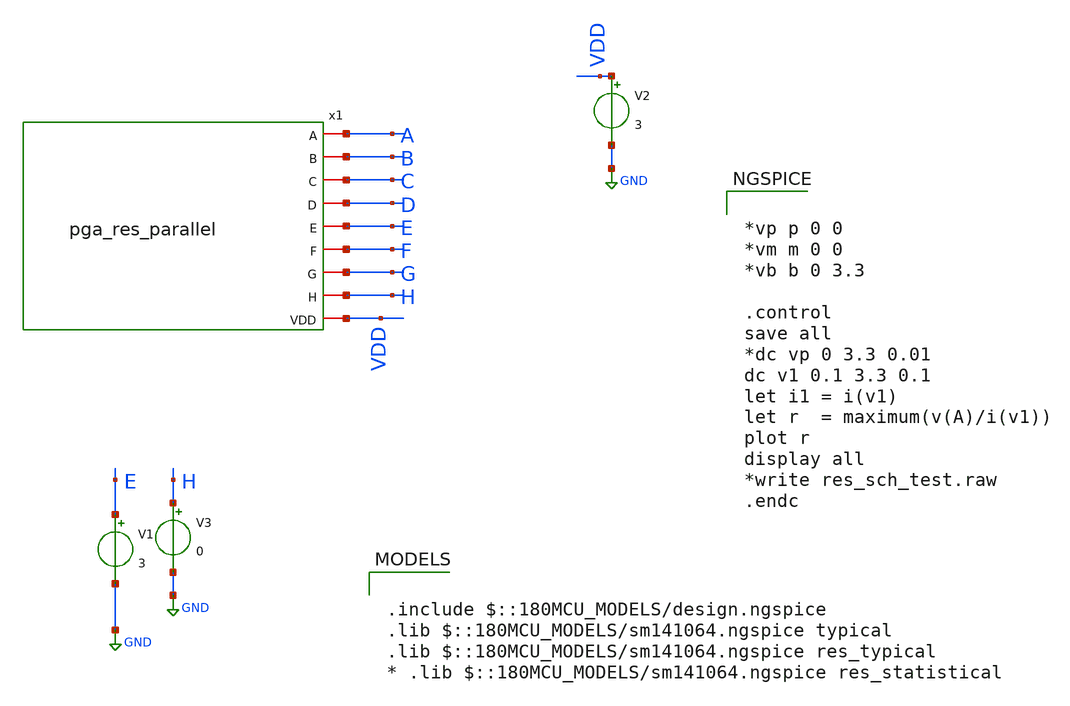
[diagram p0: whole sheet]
** sch_path: AWG_OUTPUT_AND_MUX_PAKISTAN_05/xschem/pga_parallel_tb.sch
**.subckt pga_parallel_tb
V1 E GND 3
V2 VDD GND 3
x1 A B C D E F G H VDD pga_res_parallel
V3 H GND 0
**** begin user architecture code

.include $::180MCU_MODELS/design.ngspice
.lib $::180MCU_MODELS/sm141064.ngspice typical
.lib $::180MCU_MODELS/sm141064.ngspice res_typical
* .lib $::180MCU_MODELS/sm141064.ngspice res_statistical



*vp p 0 0
*vm m 0 0
*vb b 0 3.3

.control
save all
*dc vp 0 3.3 0.01
dc v1 0.1 3.3 0.1
let i1 = i(v1)
let r  = maximum(v(A)/i(v1))
plot r
display all
*write res_sch_test.raw
.endc


**** end user architecture code
**.ends

* expanding   symbol:  pga_res_parallel.sym # of pins=9
** sym_path: AWG_OUTPUT_AND_MUX_PAKISTAN_05/xschem/pga_res_parallel.sym
** sch_path: AWG_OUTPUT_AND_MUX_PAKISTAN_05/xschem/pga_res_parallel.sch
.subckt pga_res_parallel A B C D E F G H VDD
*.iopin VDD
*.iopin A
*.iopin B
*.iopin C
*.iopin D
*.iopin E
*.iopin F
*.iopin G
*.iopin H
XR1 net1 A VDD ppolyf_u r_width=1e-6 r_length=1e-6 m=1
XR2 net2 net1 VDD ppolyf_u r_width=1e-6 r_length=1e-6 m=1
XR3 net2 net2 VDD ppolyf_u r_width=1e-6 r_length=1e-6 m=1
XR4 net2 net2 VDD ppolyf_u r_width=1e-6 r_length=1e-6 m=1
XR5 net6 net2 VDD ppolyf_u r_width=1e-6 r_length=1e-6 m=1
XR6 net3 net6 VDD ppolyf_u r_width=1e-6 r_length=1e-6 m=1
XR7 net4 net3 VDD ppolyf_u r_width=1e-6 r_length=1e-6 m=1
XR8 net7 net4 VDD ppolyf_u r_width=1e-6 r_length=1e-6 m=1
XR9 net5 net7 VDD ppolyf_u r_width=1e-6 r_length=1e-6 m=1
XR10 net78 net5 VDD ppolyf_u r_width=1e-6 r_length=1e-6 m=1
XR11 net8 net78 VDD ppolyf_u r_width=1e-6 r_length=1e-6 m=1
XR12 B net8 VDD ppolyf_u r_width=1e-6 r_length=1e-6 m=1
XR13 net9 B VDD ppolyf_u r_width=1e-6 r_length=1e-6 m=1
XR14 net14 net9 VDD ppolyf_u r_width=1e-6 r_length=1e-6 m=1
XR15 net10 net14 VDD ppolyf_u r_width=1e-6 r_length=1e-6 m=1
XR16 net11 net10 VDD ppolyf_u r_width=1e-6 r_length=1e-6 m=1
XR17 net15 net11 VDD ppolyf_u r_width=1e-6 r_length=1e-6 m=1
XR18 net12 net15 VDD ppolyf_u r_width=1e-6 r_length=1e-6 m=1
XR19 net13 net12 VDD ppolyf_u r_width=1e-6 r_length=1e-6 m=1
XR20 C net13 VDD ppolyf_u r_width=1e-6 r_length=1e-6 m=1
XR25 net16 C VDD ppolyf_u r_width=1e-6 r_length=1e-6 m=1
XR26 net22 net16 VDD ppolyf_u r_width=1e-6 r_length=1e-6 m=1
XR27 net17 net22 VDD ppolyf_u r_width=1e-6 r_length=1e-6 m=1
XR28 net18 net17 VDD ppolyf_u r_width=1e-6 r_length=1e-6 m=1
XR29 net23 net18 VDD ppolyf_u r_width=1e-6 r_length=1e-6 m=1
XR30 net19 net23 VDD ppolyf_u r_width=1e-6 r_length=1e-6 m=1
XR31 net20 net19 VDD ppolyf_u r_width=1e-6 r_length=1e-6 m=1
XR32 net24 net20 VDD ppolyf_u r_width=1e-6 r_length=1e-6 m=1
XR33 net21 net24 VDD ppolyf_u r_width=1e-6 r_length=1e-6 m=1
XR34 net79 net21 VDD ppolyf_u r_width=1e-6 r_length=1e-6 m=1
XR35 net25 net79 VDD ppolyf_u r_width=1e-6 r_length=1e-6 m=1
XR36 D net25 VDD ppolyf_u r_width=1e-6 r_length=1e-6 m=1
XR37 net26 D VDD ppolyf_u r_width=1e-6 r_length=1e-6 m=1
XR38 net32 net26 VDD ppolyf_u r_width=1e-6 r_length=1e-6 m=1
XR39 net27 net32 VDD ppolyf_u r_width=1e-6 r_length=1e-6 m=1
XR40 net28 net27 VDD ppolyf_u r_width=1e-6 r_length=1e-6 m=1
XR41 net33 net28 VDD ppolyf_u r_width=1e-6 r_length=1e-6 m=1
XR42 net29 net33 VDD ppolyf_u r_width=1e-6 r_length=1e-6 m=1
XR43 net30 net29 VDD ppolyf_u r_width=1e-6 r_length=1e-6 m=1
XR44 net34 net30 VDD ppolyf_u r_width=1e-6 r_length=1e-6 m=1
XR45 net31 net34 VDD ppolyf_u r_width=1e-6 r_length=1e-6 m=1
XR46 net77 net31 VDD ppolyf_u r_width=1e-6 r_length=1e-6 m=1
XR47 net35 net77 VDD ppolyf_u r_width=1e-6 r_length=1e-6 m=1
XR48 net73 net35 VDD ppolyf_u r_width=1e-6 r_length=1e-6 m=1
XR49 net36 E VDD ppolyf_u r_width=1e-6 r_length=1e-6 m=1
XR50 net36 net36 VDD ppolyf_u r_width=1e-6 r_length=1e-6 m=1
XR51 net37 net36 VDD ppolyf_u r_width=1e-6 r_length=1e-6 m=1
XR52 net38 net37 VDD ppolyf_u r_width=1e-6 r_length=1e-6 m=1
XR53 net42 net38 VDD ppolyf_u r_width=1e-6 r_length=1e-6 m=1
XR54 net39 net42 VDD ppolyf_u r_width=1e-6 r_length=1e-6 m=1
XR55 net40 net39 VDD ppolyf_u r_width=1e-6 r_length=1e-6 m=1
XR56 net43 net40 VDD ppolyf_u r_width=1e-6 r_length=1e-6 m=1
XR57 net41 net43 VDD ppolyf_u r_width=1e-6 r_length=1e-6 m=1
XR58 net80 net41 VDD ppolyf_u r_width=1e-6 r_length=1e-6 m=1
XR59 net44 net80 VDD ppolyf_u r_width=1e-6 r_length=1e-6 m=1
XR60 net70 net44 VDD ppolyf_u r_width=1e-6 r_length=1e-6 m=1
XR61 net45 F VDD ppolyf_u r_width=1e-6 r_length=1e-6 m=1
XR62 net51 net45 VDD ppolyf_u r_width=1e-6 r_length=1e-6 m=1
XR63 net46 net51 VDD ppolyf_u r_width=1e-6 r_length=1e-6 m=1
XR64 net47 net46 VDD ppolyf_u r_width=1e-6 r_length=1e-6 m=1
XR65 net52 net47 VDD ppolyf_u r_width=1e-6 r_length=1e-6 m=1
XR66 net48 net52 VDD ppolyf_u r_width=1e-6 r_length=1e-6 m=1
XR67 net49 net48 VDD ppolyf_u r_width=1e-6 r_length=1e-6 m=1
XR68 net53 net49 VDD ppolyf_u r_width=1e-6 r_length=1e-6 m=1
XR69 net50 net53 VDD ppolyf_u r_width=1e-6 r_length=1e-6 m=1
XR70 net81 net50 VDD ppolyf_u r_width=1e-6 r_length=1e-6 m=1
XR71 net54 net81 VDD ppolyf_u r_width=1e-6 r_length=1e-6 m=1
XR72 G net54 VDD ppolyf_u r_width=1e-6 r_length=1e-6 m=1
XR73 G G VDD ppolyf_u r_width=1e-6 r_length=1e-6 m=1
XR74 G G VDD ppolyf_u r_width=1e-6 r_length=1e-6 m=1
XR75 net55 G VDD ppolyf_u r_width=1e-6 r_length=1e-6 m=1
XR76 net56 net55 VDD ppolyf_u r_width=1e-6 r_length=1e-6 m=1
XR77 net60 net56 VDD ppolyf_u r_width=1e-6 r_length=1e-6 m=1
XR78 net57 net60 VDD ppolyf_u r_width=1e-6 r_length=1e-6 m=1
XR79 net58 net57 VDD ppolyf_u r_width=1e-6 r_length=1e-6 m=1
XR80 net61 net58 VDD ppolyf_u r_width=1e-6 r_length=1e-6 m=1
XR81 net59 net61 VDD ppolyf_u r_width=1e-6 r_length=1e-6 m=1
XR82 net82 net59 VDD ppolyf_u r_width=1e-6 r_length=1e-6 m=1
XR83 net62 net82 VDD ppolyf_u r_width=1e-6 r_length=1e-6 m=1
XR84 net83 net62 VDD ppolyf_u r_width=1e-6 r_length=1e-6 m=1
XR85 net63 net83 VDD ppolyf_u r_width=1e-6 r_length=1e-6 m=1
XR86 net68 net63 VDD ppolyf_u r_width=1e-6 r_length=1e-6 m=1
XR87 net64 net68 VDD ppolyf_u r_width=1e-6 r_length=1e-6 m=1
XR88 net65 net64 VDD ppolyf_u r_width=1e-6 r_length=1e-6 m=1
XR89 net69 net65 VDD ppolyf_u r_width=1e-6 r_length=1e-6 m=1
XR90 net66 net69 VDD ppolyf_u r_width=1e-6 r_length=1e-6 m=1
XR91 net67 net66 VDD ppolyf_u r_width=1e-6 r_length=1e-6 m=1
XR92 H net67 VDD ppolyf_u r_width=1e-6 r_length=1e-6 m=1
XR99 net71 net70 VDD ppolyf_u r_width=1e-6 r_length=1e-6 m=1
XR100 net72 net71 VDD ppolyf_u r_width=1e-6 r_length=1e-6 m=1
XR101 net76 net72 VDD ppolyf_u r_width=1e-6 r_length=1e-6 m=1
XR105 net74 net73 VDD ppolyf_u r_width=1e-6 r_length=1e-6 m=1
XR106 net75 net74 VDD ppolyf_u r_width=1e-6 r_length=1e-6 m=1
XR107 E net75 VDD ppolyf_u r_width=1e-6 r_length=1e-6 m=1
XR21 VDD VDD VDD ppolyf_u r_width=1e-6 r_length=1e-6 m=1
XR22 VDD VDD VDD ppolyf_u r_width=1e-6 r_length=1e-6 m=1
XR23 VDD VDD VDD ppolyf_u r_width=1e-6 r_length=1e-6 m=1
XR24 VDD VDD VDD ppolyf_u r_width=1e-6 r_length=1e-6 m=1
XR93 VDD VDD VDD ppolyf_u r_width=1e-6 r_length=1e-6 m=1
XR94 VDD VDD VDD ppolyf_u r_width=1e-6 r_length=1e-6 m=1
XR201 F net76 VDD ppolyf_u r_width=1e-6 r_length=1e-6 m=1
XR202 E E VDD ppolyf_u r_width=1e-6 r_length=1e-6 m=1
XR95 net84 A VDD ppolyf_u r_width=1e-6 r_length=1e-6 m=1
XR96 net85 net84 VDD ppolyf_u r_width=1e-6 r_length=1e-6 m=1
XR97 net85 net85 VDD ppolyf_u r_width=1e-6 r_length=1e-6 m=1
XR98 net85 net85 VDD ppolyf_u r_width=1e-6 r_length=1e-6 m=1
XR102 net89 net85 VDD ppolyf_u r_width=1e-6 r_length=1e-6 m=1
XR103 net86 net89 VDD ppolyf_u r_width=1e-6 r_length=1e-6 m=1
XR104 net87 net86 VDD ppolyf_u r_width=1e-6 r_length=1e-6 m=1
XR108 net90 net87 VDD ppolyf_u r_width=1e-6 r_length=1e-6 m=1
XR109 net88 net90 VDD ppolyf_u r_width=1e-6 r_length=1e-6 m=1
XR110 net161 net88 VDD ppolyf_u r_width=1e-6 r_length=1e-6 m=1
XR111 net91 net161 VDD ppolyf_u r_width=1e-6 r_length=1e-6 m=1
XR112 B net91 VDD ppolyf_u r_width=1e-6 r_length=1e-6 m=1
XR113 net92 B VDD ppolyf_u r_width=1e-6 r_length=1e-6 m=1
XR114 net97 net92 VDD ppolyf_u r_width=1e-6 r_length=1e-6 m=1
XR115 net93 net97 VDD ppolyf_u r_width=1e-6 r_length=1e-6 m=1
XR116 net94 net93 VDD ppolyf_u r_width=1e-6 r_length=1e-6 m=1
XR117 net98 net94 VDD ppolyf_u r_width=1e-6 r_length=1e-6 m=1
XR118 net95 net98 VDD ppolyf_u r_width=1e-6 r_length=1e-6 m=1
XR119 net96 net95 VDD ppolyf_u r_width=1e-6 r_length=1e-6 m=1
XR120 C net96 VDD ppolyf_u r_width=1e-6 r_length=1e-6 m=1
XR121 net99 C VDD ppolyf_u r_width=1e-6 r_length=1e-6 m=1
XR122 net105 net99 VDD ppolyf_u r_width=1e-6 r_length=1e-6 m=1
XR123 net100 net105 VDD ppolyf_u r_width=1e-6 r_length=1e-6 m=1
XR124 net101 net100 VDD ppolyf_u r_width=1e-6 r_length=1e-6 m=1
XR125 net106 net101 VDD ppolyf_u r_width=1e-6 r_length=1e-6 m=1
XR126 net102 net106 VDD ppolyf_u r_width=1e-6 r_length=1e-6 m=1
XR127 net103 net102 VDD ppolyf_u r_width=1e-6 r_length=1e-6 m=1
XR128 net107 net103 VDD ppolyf_u r_width=1e-6 r_length=1e-6 m=1
XR129 net104 net107 VDD ppolyf_u r_width=1e-6 r_length=1e-6 m=1
XR130 net162 net104 VDD ppolyf_u r_width=1e-6 r_length=1e-6 m=1
XR131 net108 net162 VDD ppolyf_u r_width=1e-6 r_length=1e-6 m=1
XR132 D net108 VDD ppolyf_u r_width=1e-6 r_length=1e-6 m=1
XR133 net109 D VDD ppolyf_u r_width=1e-6 r_length=1e-6 m=1
XR134 net115 net109 VDD ppolyf_u r_width=1e-6 r_length=1e-6 m=1
XR135 net110 net115 VDD ppolyf_u r_width=1e-6 r_length=1e-6 m=1
XR136 net111 net110 VDD ppolyf_u r_width=1e-6 r_length=1e-6 m=1
XR137 net116 net111 VDD ppolyf_u r_width=1e-6 r_length=1e-6 m=1
XR138 net112 net116 VDD ppolyf_u r_width=1e-6 r_length=1e-6 m=1
XR139 net113 net112 VDD ppolyf_u r_width=1e-6 r_length=1e-6 m=1
XR140 net117 net113 VDD ppolyf_u r_width=1e-6 r_length=1e-6 m=1
XR141 net114 net117 VDD ppolyf_u r_width=1e-6 r_length=1e-6 m=1
XR142 net160 net114 VDD ppolyf_u r_width=1e-6 r_length=1e-6 m=1
XR143 net118 net160 VDD ppolyf_u r_width=1e-6 r_length=1e-6 m=1
XR144 net156 net118 VDD ppolyf_u r_width=1e-6 r_length=1e-6 m=1
XR145 net119 E VDD ppolyf_u r_width=1e-6 r_length=1e-6 m=1
XR146 net119 net119 VDD ppolyf_u r_width=1e-6 r_length=1e-6 m=1
XR147 net120 net119 VDD ppolyf_u r_width=1e-6 r_length=1e-6 m=1
XR148 net121 net120 VDD ppolyf_u r_width=1e-6 r_length=1e-6 m=1
XR149 net125 net121 VDD ppolyf_u r_width=1e-6 r_length=1e-6 m=1
XR150 net122 net125 VDD ppolyf_u r_width=1e-6 r_length=1e-6 m=1
XR151 net123 net122 VDD ppolyf_u r_width=1e-6 r_length=1e-6 m=1
XR152 net126 net123 VDD ppolyf_u r_width=1e-6 r_length=1e-6 m=1
XR153 net124 net126 VDD ppolyf_u r_width=1e-6 r_length=1e-6 m=1
XR154 net163 net124 VDD ppolyf_u r_width=1e-6 r_length=1e-6 m=1
XR155 net127 net163 VDD ppolyf_u r_width=1e-6 r_length=1e-6 m=1
XR156 net153 net127 VDD ppolyf_u r_width=1e-6 r_length=1e-6 m=1
XR157 net128 F VDD ppolyf_u r_width=1e-6 r_length=1e-6 m=1
XR158 net134 net128 VDD ppolyf_u r_width=1e-6 r_length=1e-6 m=1
XR159 net129 net134 VDD ppolyf_u r_width=1e-6 r_length=1e-6 m=1
XR160 net130 net129 VDD ppolyf_u r_width=1e-6 r_length=1e-6 m=1
XR161 net135 net130 VDD ppolyf_u r_width=1e-6 r_length=1e-6 m=1
XR162 net131 net135 VDD ppolyf_u r_width=1e-6 r_length=1e-6 m=1
XR163 net132 net131 VDD ppolyf_u r_width=1e-6 r_length=1e-6 m=1
XR164 net136 net132 VDD ppolyf_u r_width=1e-6 r_length=1e-6 m=1
XR165 net133 net136 VDD ppolyf_u r_width=1e-6 r_length=1e-6 m=1
XR166 net164 net133 VDD ppolyf_u r_width=1e-6 r_length=1e-6 m=1
XR167 net137 net164 VDD ppolyf_u r_width=1e-6 r_length=1e-6 m=1
XR168 G net137 VDD ppolyf_u r_width=1e-6 r_length=1e-6 m=1
XR169 G G VDD ppolyf_u r_width=1e-6 r_length=1e-6 m=1
XR170 G G VDD ppolyf_u r_width=1e-6 r_length=1e-6 m=1
XR171 net138 G VDD ppolyf_u r_width=1e-6 r_length=1e-6 m=1
XR172 net139 net138 VDD ppolyf_u r_width=1e-6 r_length=1e-6 m=1
XR173 net143 net139 VDD ppolyf_u r_width=1e-6 r_length=1e-6 m=1
XR174 net140 net143 VDD ppolyf_u r_width=1e-6 r_length=1e-6 m=1
XR175 net141 net140 VDD ppolyf_u r_width=1e-6 r_length=1e-6 m=1
XR176 net144 net141 VDD ppolyf_u r_width=1e-6 r_length=1e-6 m=1
XR177 net142 net144 VDD ppolyf_u r_width=1e-6 r_length=1e-6 m=1
XR178 net165 net142 VDD ppolyf_u r_width=1e-6 r_length=1e-6 m=1
XR179 net145 net165 VDD ppolyf_u r_width=1e-6 r_length=1e-6 m=1
XR180 net166 net145 VDD ppolyf_u r_width=1e-6 r_length=1e-6 m=1
XR181 net146 net166 VDD ppolyf_u r_width=1e-6 r_length=1e-6 m=1
XR182 net151 net146 VDD ppolyf_u r_width=1e-6 r_length=1e-6 m=1
XR183 net147 net151 VDD ppolyf_u r_width=1e-6 r_length=1e-6 m=1
XR184 net148 net147 VDD ppolyf_u r_width=1e-6 r_length=1e-6 m=1
XR185 net152 net148 VDD ppolyf_u r_width=1e-6 r_length=1e-6 m=1
XR186 net149 net152 VDD ppolyf_u r_width=1e-6 r_length=1e-6 m=1
XR187 net150 net149 VDD ppolyf_u r_width=1e-6 r_length=1e-6 m=1
XR188 H net150 VDD ppolyf_u r_width=1e-6 r_length=1e-6 m=1
XR189 net154 net153 VDD ppolyf_u r_width=1e-6 r_length=1e-6 m=1
XR190 net155 net154 VDD ppolyf_u r_width=1e-6 r_length=1e-6 m=1
XR191 net159 net155 VDD ppolyf_u r_width=1e-6 r_length=1e-6 m=1
XR192 net157 net156 VDD ppolyf_u r_width=1e-6 r_length=1e-6 m=1
XR193 net158 net157 VDD ppolyf_u r_width=1e-6 r_length=1e-6 m=1
XR194 E net158 VDD ppolyf_u r_width=1e-6 r_length=1e-6 m=1
XR195 VDD VDD VDD ppolyf_u r_width=1e-6 r_length=1e-6 m=1
XR196 VDD VDD VDD ppolyf_u r_width=1e-6 r_length=1e-6 m=1
XR197 VDD VDD VDD ppolyf_u r_width=1e-6 r_length=1e-6 m=1
XR198 VDD VDD VDD ppolyf_u r_width=1e-6 r_length=1e-6 m=1
XR199 VDD VDD VDD ppolyf_u r_width=1e-6 r_length=1e-6 m=1
XR200 VDD VDD VDD ppolyf_u r_width=1e-6 r_length=1e-6 m=1
XR203 F net159 VDD ppolyf_u r_width=1e-6 r_length=1e-6 m=1
XR204 E E VDD ppolyf_u r_width=1e-6 r_length=1e-6 m=1
.ends

.GLOBAL GND
.end
